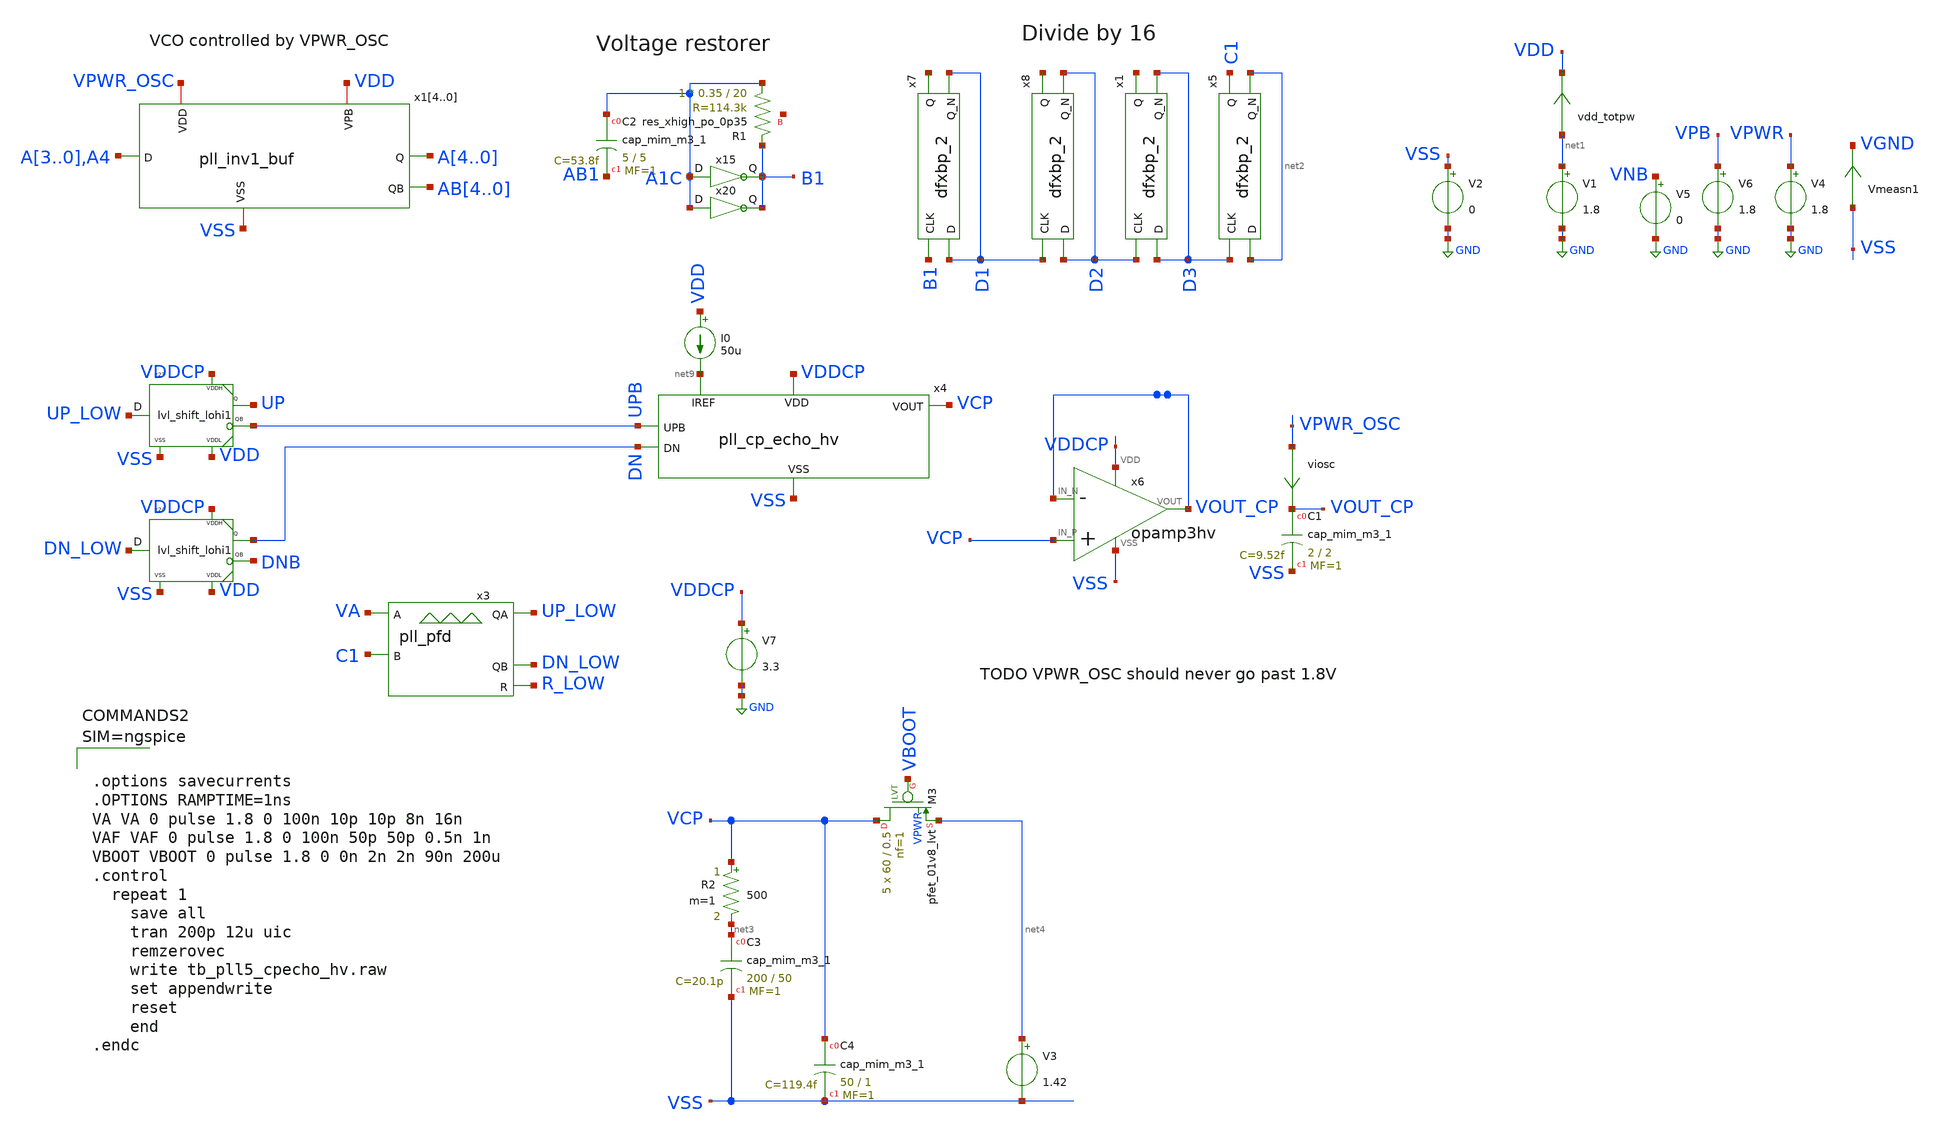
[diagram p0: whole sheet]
** sch_path: xschem/tb_pll5_cpecho_hv.sch
**.subckt tb_pll5_cpecho_hv
V5 VNB GND 0
V6 VPB GND 1.8
V1 net1 GND 1.8
V2 VSS GND 0
vdd_totpw net1 VDD 0
.save i(vdd_totpw)
Vmeasn1 VSS VGND 0
.save i(vmeasn1)
x3 VA C1 UP_LOW DN_LOW R_LOW VDD VSS pll_pfd
x7 B1 D1 VGND VNB VPB VPWR net5 D1 sky130_fd_sc_hd__dfxbp_2
x8 D1 D2 VGND VNB VPB VPWR net6 D2 sky130_fd_sc_hd__dfxbp_2
V4 VPWR GND 1.8
x1 D2 D3 VGND VNB VPB VPWR net7 D3 sky130_fd_sc_hd__dfxbp_2
x5 D3 net2 VGND VNB VPB VPWR C1 net2 sky130_fd_sc_hd__dfxbp_2
V7 VDDCP GND 3.3
x15 A1C B1 VDD VSS pll_inv1
XR1 A1C B1 net8 sky130_fd_pr__res_xhigh_po_0p35 L=20 mult=1 m=1
XC2 A1C AB1 sky130_fd_pr__cap_mim_m3_1 W=5 L=5 MF=1 m=1
viosc VPWR_OSC VOUT_CP 0
.save i(viosc)
V3 net4 VSS 1.42
x6 VDDCP VCP VOUT_CP VOUT_CP VSS opamp3hv
x23 UP_LOW UP UPB VDDCP VDD VSS lvl_shift_lohi1
x24 DN_LOW DN DNB VDDCP VDD VSS lvl_shift_lohi1
XC1 VOUT_CP VSS sky130_fd_pr__cap_mim_m3_1 W=2 L=2 MF=1 m=1
x14 A3 A4 AB4 VDD VPWR_OSC VSS pll_inv1_buf
x13 A2 A3 AB3 VDD VPWR_OSC VSS pll_inv1_buf
x12 A1 A2 AB2 VDD VPWR_OSC VSS pll_inv1_buf
x11 A0 A1 AB1 VDD VPWR_OSC VSS pll_inv1_buf
x10 A4 A0 AB0 VDD VPWR_OSC VSS pll_inv1_buf
x20 A1C B1 VDD VSS pll_inv1
x4 VDDCP DN VCP VSS UPB net9 pll_cp_echo_hv
I0 VDD net9 50u
XC3 net3 VSS sky130_fd_pr__cap_mim_m3_1 W=200 L=50 MF=1 m=1
R2 VCP net3 500 m=1
XC4 VCP VSS sky130_fd_pr__cap_mim_m3_1 W=50 L=1 MF=1 m=1
XM3 VCP VBOOT net4 VPWR sky130_fd_pr__pfet_01v8_lvt L=0.5 W=60 nf=1 ad='int((nf+1)/2) * W/nf * 0.29'
+ as='int((nf+2)/2) * W/nf * 0.29' pd='2*int((nf+1)/2) * (W/nf + 0.29)' ps='2*int((nf+2)/2) * (W/nf + 0.29)'
+ nrd='0.29 / W' nrs='0.29 / W' sa=0 sb=0 sd=0 mult=5 m=5
**** begin user architecture code

** opencircuitdesign pdks install
.lib $::SKYWATER_MODELS/sky130.lib.spice tt
.include $::SKYWATER_STDCELLS/sky130_fd_sc_hd.spice





.options savecurrents
.OPTIONS RAMPTIME=1ns
VA VA 0 pulse 1.8 0 100n 10p 10p 8n 16n
VAF VAF 0 pulse 1.8 0 100n 50p 50p 0.5n 1n
VBOOT VBOOT 0 pulse 1.8 0 0n 2n 2n 90n 200u
.control
  repeat 1
    save all
    tran 200p 12u uic
    remzerovec
    write tb_pll5_cpecho_hv.raw
    set appendwrite
    reset
    end
.endc



**** end user architecture code
**.ends
.GLOBAL GND
.end
